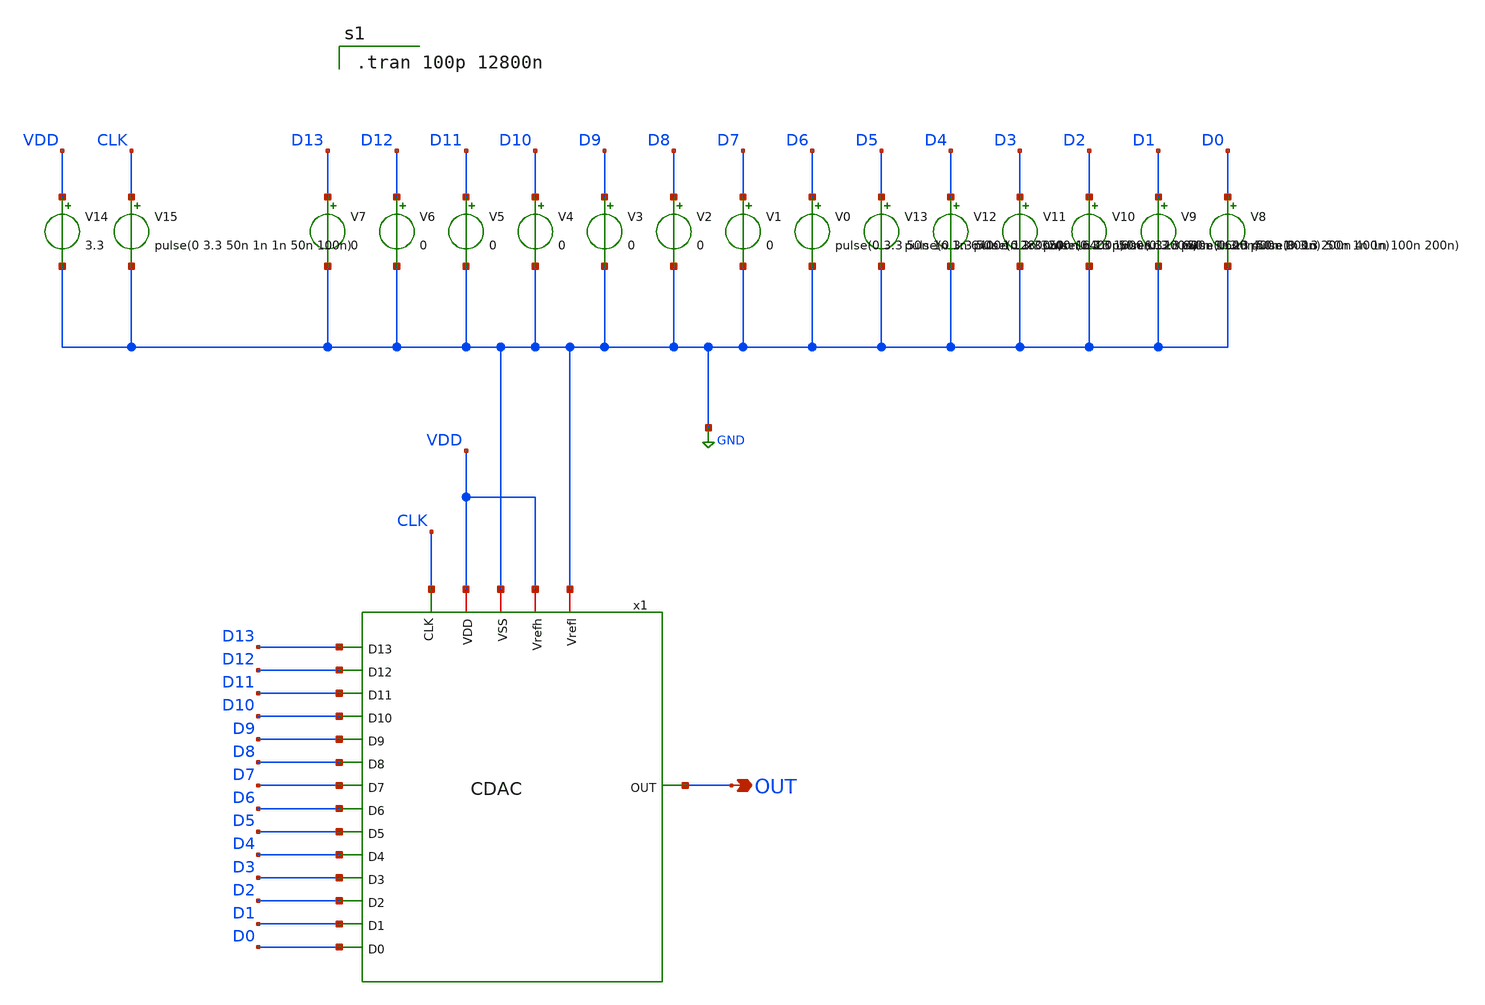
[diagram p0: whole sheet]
** sch_path: CDAC_sim.sch
**.subckt CDAC_sim OUT
*.opin OUT
x1 CLK D11 D13 D12 D7 D10 D1 D0 D9 D8 D2 D6 D5 D4 D3 OUT GND VDD GND VDD CDAC
V14 VDD GND 3.3
V15 CLK GND pulse(0 3.3 50n 1n 1n 50n 100n)
V13 D5 GND pulse(0 3.3 50n 1n 1n 3200n 6400n)
V12 D4 GND pulse(0 3.3 50n 1n 1n 1600n 3200n)
V11 D3 GND pulse(0 3.3 50n 1n 1n 800n 1600n)
V10 D2 GND pulse(0 3.3 50n 1n 1n 400n 800n)
V9 D1 GND pulse(0 3.3 50n 1n 1n 200n 400n)
V8 D0 GND pulse(0 3.3 50n 1n 1n 100n 200n)
V7 D13 GND 0
V6 D12 GND 0
V5 D11 GND 0
V4 D10 GND 0
V3 D9 GND 0
V2 D8 GND 0
V1 D7 GND 0
V0 D6 GND pulse(0 3.3 50n 1n 1n 6400n 12800n)
**** begin user architecture code

.tran 100p 12800n

**** end user architecture code
**.ends

* expanding   symbol:  C:/Users/ISLab2/Documents/minimal_LR/CDAC.sym # of pins=20
** sym_path: CDAC.sym
** sch_path: CDAC.sch
.subckt CDAC CLK D11 D13 D12 D7 D10 D1 D0 D9 D8 D2 D6 D5 D4 D3 OUT VSS VDD Vrefl Vrefh
*.opin OUT
*.iopin Vrefh
*.iopin Vrefl
*.ipin D13
*.ipin D12
*.ipin D11
*.ipin D10
*.iopin VSS
*.iopin VDD
*.ipin D9
*.ipin D8
*.ipin D7
*.ipin D6
*.ipin D5
*.ipin D4
*.ipin D3
*.ipin D2
*.ipin D1
*.ipin D0
*.ipin CLK
C1 OUT Vrefl 10f m=1
C2 OUT net1 10f m=1
C3 OUT net2 20f m=1
C4 OUT net4 40f m=1
C5 OUT net3 80f m=1
x2 D0bO VSS net1 Vrefl VDD CMOSSW
x3 D0A VSS net1 Vrefh VDD CMOSSW
x4 D1bO VSS net2 Vrefl VDD CMOSSW
x5 D1A VSS net2 Vrefh VDD CMOSSW
x6 D3bO VSS net3 Vrefl VDD CMOSSW
x7 D3A VSS net3 Vrefh VDD CMOSSW
x8 D2bO VSS net4 Vrefl VDD CMOSSW
x9 D2A VSS net4 Vrefh VDD CMOSSW
x15 VDD D13b D13 VSS INV
x16 VDD D12b D12 VSS INV
x17 VDD D11b D11 VSS INV
x18 VDD D10b D10 VSS INV
C6 OUT net5 0.16p m=1
C7 OUT net6 0.32p m=1
C8 OUT net8 0.64p m=1
C9 OUT net7 1.28p m=1
x1 D4bO VSS net5 Vrefl VDD CMOSSW
x11 D4A VSS net5 Vrefh VDD CMOSSW
x12 D5bO VSS net6 Vrefl VDD CMOSSW
x13 D5A VSS net6 Vrefh VDD CMOSSW
x14 D7bO VSS net7 Vrefl VDD CMOSSW
x19 D7A VSS net7 Vrefh VDD CMOSSW
x20 D6bO VSS net8 Vrefl VDD CMOSSW
x21 D6A VSS net8 Vrefh VDD CMOSSW
C10 OUT net10 2.56p m=1
C11 OUT net9 5.12p m=1
x22 D9bO VSS net9 Vrefl VDD CMOSSW
x23 D9A VSS net9 Vrefh VDD CMOSSW
x24 D8bO VSS net10 Vrefl VDD CMOSSW
x25 D8A VSS net10 Vrefh VDD CMOSSW
C12 OUT net11 10.24p m=1
C13 OUT net12 20.48p m=1
C14 OUT net14 40.96p m=1
C15 OUT net13 81.92p m=1
x34 VDD D9b D9 VSS INV
x35 VDD D8b D8 VSS INV
x36 VDD D7b D7 VSS INV
x37 VDD D6b D6 VSS INV
x38 VDD D5b D5 VSS INV
x39 VDD D4b D4 VSS INV
x40 VDD D3b D3 VSS INV
x41 VDD D2b D2 VSS INV
x42 VDD D1b D1 VSS INV
x43 VDD D0b D0 VSS INV
x44 VDD D13A CLK2 D13 VSS AND
x45 VDD D12A CLK2 D12 VSS AND
x46 VDD D11A CLK2 D11 VSS AND
x47 VDD D10A CLK2 D10 VSS AND
x48 VDD D9A CLK2 D9 VSS AND
x49 VDD D8A CLK2 D8 VSS AND
x50 VDD D7A CLK2 D7 VSS AND
x51 VDD D6A CLK2 D6 VSS AND
x52 VDD D5A CLK2 D5 VSS AND
x53 VDD D4A CLK2 D4 VSS AND
x54 VDD D3A CLK2 D3 VSS AND
x55 VDD D2A CLK2 D2 VSS AND
x56 VDD D1A CLK2 D1 VSS AND
x57 VDD D0A CLK2 D0 VSS AND
x58 VDD CLK1 D13bO D13b VSS OR
x59 VDD CLK1 D12bO D12b VSS OR
x60 VDD CLK1 D11bO D11b VSS OR
x61 VDD CLK1 D10bO D10b VSS OR
x62 VDD CLK1 D9bO D9b VSS OR
x63 VDD CLK1 D8bO D8b VSS OR
x64 VDD CLK1 D7bO D7b VSS OR
x65 VDD CLK1 D6bO D6b VSS OR
x66 VDD CLK1 D5bO D5b VSS OR
x67 VDD CLK1 D4bO D4b VSS OR
x68 VDD CLK1 D3bO D3b VSS OR
x69 VDD CLK1 D2bO D2b VSS OR
x70 VDD CLK1 D1bO D1b VSS OR
x71 VDD CLK1 D0bO D0b VSS OR
x72 VDD CLK CLK1 VSS CLK2 NOL
x30 D13A VSS net13 Vrefh VDD CMOSSW16
x31 D13bO VSS net13 Vrefl VDD CMOSSW16
x33 D12A VSS net14 Vrefh VDD CMOSSW8
x32 D12bO VSS net14 Vrefl VDD CMOSSW8
x28 D11A VSS net12 Vrefh VDD CMOSSW4
x29 D11bO VSS net12 Vrefl VDD CMOSSW4
x26 D10A VSS net11 Vrefh VDD CMOSSW2
x27 D10bO VSS net11 Vrefl VDD CMOSSW2
x10 CLK1 VSS OUT Vrefl VDD CMOSSW16
.ends


* expanding   symbol:  C:/Users/ISLab2/Documents/minimal_LR/CMOSSW.sym # of pins=5
** sym_path: CMOSSW.sym
** sch_path: CMOSSW.sch
.subckt CMOSSW CLK VSS OUT IN VDD
*.ipin IN
*.iopin VDD
*.iopin VSS
*.opin OUT
*.iopin CLK
M1 OUT CLK IN VSS nch w=10u l=0.35u as=0 ps=0 ad=0 pd=0 m=1
M2 OUT net1 IN VDD pch w=10u l=0.35u as=0 ps=0 ad=0 pd=0 m=1
**** begin user architecture code


.include C:/Users/ISLab2/Documents/minimal_LR/minimal.txt

**** end user architecture code
x1 VDD net1 CLK VSS INV
.ends


* expanding   symbol:  C:/Users/ISLab2/Documents/minimal_LR/INV.sym # of pins=4
** sym_path: INV.sym
** sch_path: INV.sch
.subckt INV VDD OUT IN VSS
*.opin OUT
*.ipin IN
*.iopin VDD
*.iopin VSS
M2 OUT IN VDD VDD pch w=10u l=0.35u as=0 ps=0 ad=0 pd=0 m=1
M1 OUT IN VSS VSS nch w=5u l=0.35u as=0 ps=0 ad=0 pd=0 m=1
.ends


* expanding   symbol:  C:/Users/ISLab2/Documents/minimal_LR/AND.sym # of pins=5
** sym_path: AND.sym
** sch_path: AND.sch
.subckt AND VDD Y A B VSS
*.iopin VDD
*.ipin A
*.ipin B
*.iopin VSS
*.opin Y
M1 net1 A net2 VSS nch w=3.5u l=0.35u as=0 ps=0 ad=0 pd=0 m=1
M2 net1 B VDD VDD pch w=3.5u l=0.35u as=0 ps=0 ad=0 pd=0 m=1
M3 net1 A VDD VDD pch w=3.5u l=0.35u as=0 ps=0 ad=0 pd=0 m=1
M4 net2 B VSS VSS nch w=3.5u l=0.35u as=0 ps=0 ad=0 pd=0 m=1
M5 Y net1 VDD VDD pch w=3.5u l=0.35u as=0 ps=0 ad=0 pd=0 m=1
M6 Y net1 VSS VSS nch w=3.5u l=0.35u as=0 ps=0 ad=0 pd=0 m=1
.ends


* expanding   symbol:  C:/Users/ISLab2/Documents/minimal_LR/OR.sym # of pins=5
** sym_path: OR.sym
** sch_path: OR.sch
.subckt OR VDD A Y B VSS
*.iopin VDD
*.ipin A
*.ipin B
*.iopin VSS
*.opin Y
M1 net1 A VSS VSS nch w=3.5u l=0.35u as=0 ps=0 ad=0 pd=0 m=1
M2 net2 A VDD VDD pch w=3.5u l=0.35u as=0 ps=0 ad=0 pd=0 m=1
M3 net1 B net2 VDD pch w=3.5u l=0.35u as=0 ps=0 ad=0 pd=0 m=1
M4 net1 B VSS VSS nch w=3.5u l=0.35u as=0 ps=0 ad=0 pd=0 m=1
M5 Y net1 VDD VDD pch w=3.5u l=0.35u as=0 ps=0 ad=0 pd=0 m=1
M6 Y net1 VSS VSS nch w=3.5u l=0.35u as=0 ps=0 ad=0 pd=0 m=1
.ends


* expanding   symbol:  C:/Users/ISLab2/Documents/minimal_LR/NOL.sym # of pins=5
** sym_path: NOL.sym
** sch_path: NOL.sch
.subckt NOL VDD CLK CLK1 VSS CLK2
*.ipin CLK
*.opin CLK1
*.opin CLK2
*.iopin VDD
*.iopin VSS
x3 VDD net1 CLK VSS INV
x1 VDD CLK net9 CLK2 VSS NOR
x2 VDD CLK1 net2 net1 VSS NOR
x4 VDD net3 net2 VSS INV
x5 VDD net4 net3 VSS INV
x6 VDD net5 net4 VSS INV
x7 VDD net17 net5 VSS INV
x8 VDD net6 net9 VSS INV
x9 VDD net7 net6 VSS INV
x10 VDD net8 net7 VSS INV
x11 VDD net13 net8 VSS INV
x12 VDD net10 net13 VSS INV
x13 VDD net11 net10 VSS INV
x14 VDD net12 net11 VSS INV
x15 VDD net32 net12 VSS INV
x16 VDD net14 net17 VSS INV
x17 VDD net15 net14 VSS INV
x18 VDD net16 net15 VSS INV
x19 VDD net33 net16 VSS INV
x20 VDD net18 net33 VSS INV
x21 VDD net19 net18 VSS INV
x22 VDD net20 net19 VSS INV
x23 VDD net24 net20 VSS INV
x24 VDD net21 net24 VSS INV
x25 VDD net22 net21 VSS INV
x26 VDD net23 net22 VSS INV
x27 VDD CLK2 net23 VSS INV
x28 VDD net25 net32 VSS INV
x29 VDD net26 net25 VSS INV
x30 VDD net27 net26 VSS INV
x31 VDD net31 net27 VSS INV
x32 VDD net28 net31 VSS INV
x33 VDD net29 net28 VSS INV
x34 VDD net30 net29 VSS INV
x35 VDD CLK1 net30 VSS INV
.ends


* expanding   symbol:  C:/Users/ISLab2/Documents/minimal_LR/CMOSSW16.sym # of pins=5
** sym_path: CMOSSW16.sym
** sch_path: CMOSSW16.sch
.subckt CMOSSW16 CLK VSS OUT IN VDD
*.ipin IN
*.opin OUT
*.iopin VSS
*.iopin VDD
*.iopin CLK
x1 CLK VSS OUT IN VDD CMOSSW8
x2 CLK VSS OUT IN VDD CMOSSW8
.ends


* expanding   symbol:  C:/Users/ISLab2/Documents/minimal_LR/CMOSSW8.sym # of pins=5
** sym_path: CMOSSW8.sym
** sch_path: CMOSSW8.sch
.subckt CMOSSW8 CLK VSS OUT IN VDD
*.ipin IN
*.opin OUT
*.iopin VSS
*.iopin VDD
*.iopin CLK
x1 CLK VSS OUT IN VDD CMOSSW4
x2 CLK VSS OUT IN VDD CMOSSW4
.ends


* expanding   symbol:  C:/Users/ISLab2/Documents/minimal_LR/CMOSSW4.sym # of pins=5
** sym_path: CMOSSW4.sym
** sch_path: CMOSSW4.sch
.subckt CMOSSW4 CLK VSS OUT IN VDD
*.ipin IN
*.opin OUT
*.iopin VSS
*.iopin VDD
*.iopin CLK
x1 CLK VSS OUT IN VDD CMOSSW2
x2 CLK VSS OUT IN VDD CMOSSW2
.ends


* expanding   symbol:  C:/Users/ISLab2/Documents/minimal_LR/CMOSSW2.sym # of pins=5
** sym_path: CMOSSW2.sym
** sch_path: CMOSSW2.sch
.subckt CMOSSW2 CLK VSS OUT IN VDD
*.ipin IN
*.opin OUT
*.iopin VSS
*.iopin VDD
*.iopin CLK
x1 CLK VSS OUT IN VDD CMOSSW
x2 CLK VSS OUT IN VDD CMOSSW
.ends


* expanding   symbol:  C:/Users/ISLab2/Documents/minimal_LR/NOR.sym # of pins=5
** sym_path: NOR.sym
** sch_path: NOR.sch
.subckt NOR VDD A Y B VSS
*.iopin VDD
*.ipin A
*.ipin B
*.iopin VSS
*.opin Y
M1 Y A VSS VSS nch w=3.5u l=0.35u as=0 ps=0 ad=0 pd=0 m=1
M2 net1 A VDD VDD pch w=3.5u l=0.35u as=0 ps=0 ad=0 pd=0 m=1
M3 Y B net1 VDD pch w=3.5u l=0.35u as=0 ps=0 ad=0 pd=0 m=1
M4 Y B VSS VSS nch w=3.5u l=0.35u as=0 ps=0 ad=0 pd=0 m=1
**** begin user architecture code


.include C:/Users/ISLab2/Documents/minimal_LR/minimal.txt

**** end user architecture code
.ends

.GLOBAL GND
.end
